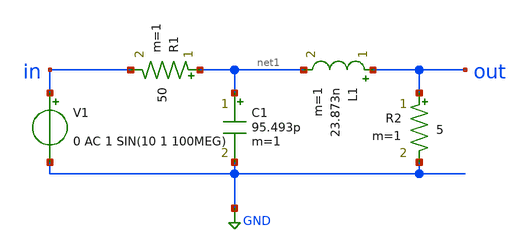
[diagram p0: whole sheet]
** sch_path: circuits-pub/RF/RLC_Networks/Impedance_Matching/L_match.sch
**.subckt L_match
V1 in GND 0 AC 1 SIN(10 1 100MEG)
C1 net1 GND 95.493p m=1
R1 net1 in 50 m=1
L1 out net1 23.873n m=1
R2 out GND 5 m=1
**** begin user architecture code


.control

tran 0.1n 100n
plot v(out)


.endc




**** end user architecture code
**.ends
.GLOBAL GND
.end
